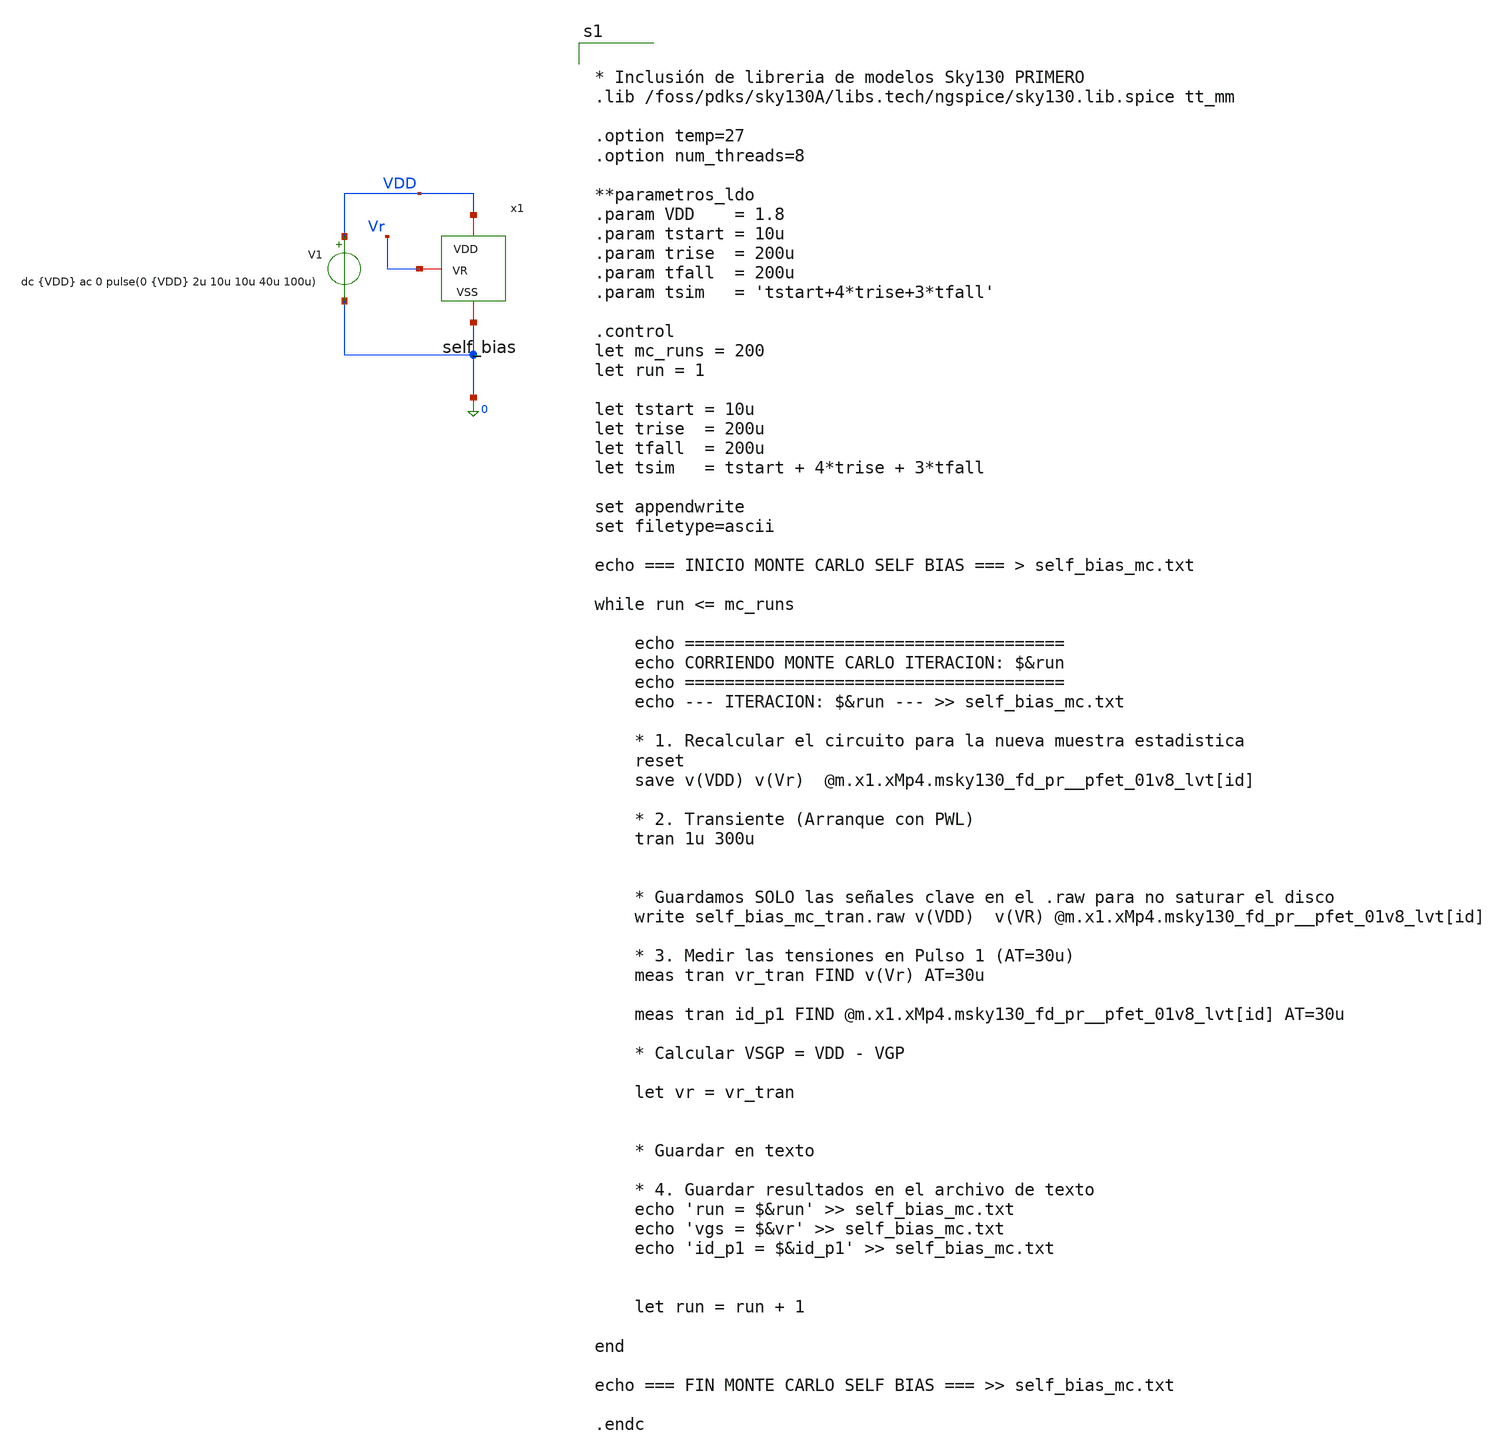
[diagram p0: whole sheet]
** sch_path: xschem/Iref/self_bias_tb_mc.sch
**.subckt self_bias_tb_mc
V1 VDD 0 dc {VDD} ac 0 pulse(0 {VDD} 2u 10u 10u 40u 100u)
x1 VDD Vr 0 self_bias
**** begin user architecture code


* Inclusión de libreria de modelos Sky130 PRIMERO
.lib /foss/pdks/sky130A/libs.tech/ngspice/sky130.lib.spice tt_mm

.option temp=27
.option num_threads=8

**parametros_ldo
.param VDD    = 1.8
.param tstart = 10u
.param trise  = 200u
.param tfall  = 200u
.param tsim   = 'tstart+4*trise+3*tfall'

.control
let mc_runs = 200
let run = 1

let tstart = 10u
let trise  = 200u
let tfall  = 200u
let tsim   = tstart + 4*trise + 3*tfall

set appendwrite
set filetype=ascii

echo === INICIO MONTE CARLO SELF BIAS === > self_bias_mc.txt

while run <= mc_runs

    echo ======================================
    echo CORRIENDO MONTE CARLO ITERACION: $&run
    echo ======================================
    echo --- ITERACION: $&run --- >> self_bias_mc.txt

    * 1. Recalcular el circuito para la nueva muestra estadistica
    reset
    save v(VDD) v(Vr)  @m.x1.xMp4.msky130_fd_pr__pfet_01v8_lvt[id]

    * 2. Transiente (Arranque con PWL)
    tran 1u 300u


    * Guardamos SOLO las señales clave en el .raw para no saturar el disco
    write self_bias_mc_tran.raw v(VDD)  v(VR) @m.x1.xMp4.msky130_fd_pr__pfet_01v8_lvt[id]

    * 3. Medir las tensiones en Pulso 1 (AT=30u)
    meas tran vr_tran FIND v(Vr) AT=30u

    meas tran id_p1 FIND @m.x1.xMp4.msky130_fd_pr__pfet_01v8_lvt[id] AT=30u

    * Calcular VSGP = VDD - VGP

    let vr = vr_tran


    * Guardar en texto

    * 4. Guardar resultados en el archivo de texto
    echo 'run = $&run' >> self_bias_mc.txt
    echo 'vgs = $&vr' >> self_bias_mc.txt
    echo 'id_p1 = $&id_p1' >> self_bias_mc.txt


    let run = run + 1

end

echo === FIN MONTE CARLO SELF BIAS === >> self_bias_mc.txt

.endc


**** end user architecture code
**.ends

* expanding   symbol:  self_bias.sym # of pins=3
** sym_path: xschem/Iref/self_bias.sym
** sch_path: xschem/Iref/self_bias.sch
.subckt self_bias VDD VR VSS
*.iopin VR
*.iopin VDD
*.iopin VSS
XMp4 Vgp Vgp VDD VDD sky130_fd_pr__pfet_01v8_lvt L=1 W=30 nf=1 ad='int((1 + 1)/2) * 30 / 1 * 0.29' as='int((1 + 2)/2) * 30 / 1 * 0.29'
+ pd='2*int((1 + 1)/2) * (30 / 1 + 0.29)' ps='2*int((1 + 2)/2) * (30 / 1 + 0.29)' nrd='0.29 / 30 ' nrs='0.29 / 30 '
+ sa=0 sb=0 sd=0 mult=1 m=1
XMp3 VDI Vgp VDD VDD sky130_fd_pr__pfet_01v8_lvt L=1 W=30 nf=1 ad='int((1 + 1)/2) * 30 / 1 * 0.29' as='int((1 + 2)/2) * 30 / 1 * 0.29'
+ pd='2*int((1 + 1)/2) * (30 / 1 + 0.29)' ps='2*int((1 + 2)/2) * (30 / 1 + 0.29)' nrd='0.29 / 30 ' nrs='0.29 / 30 '
+ sa=0 sb=0 sd=0 mult=1 m=1
XMs2 VDinv VR VDD VDD sky130_fd_pr__pfet_01v8_lvt L=25 W=0.5 nf=1 ad='int((1 + 1)/2) * 0.5 / 1 * 0.29'
+ as='int((1 + 2)/2) * 0.5 / 1 * 0.29' pd='2*int((1 + 1)/2) * (0.5 / 1 + 0.29)' ps='2*int((1 + 2)/2) * (0.5 / 1 + 0.29)'
+ nrd='0.29 / 0.5 ' nrs='0.29 / 0.5 ' sa=0 sb=0 sd=0 mult=1 m=1
XR4 VSS VR VSS sky130_fd_pr__res_iso_pw W=0.7 L=11 m=1
XMn2 Vgp VDI VR VSS sky130_fd_pr__nfet_01v8 L=1 W=20 nf=1 ad='int((1 + 1)/2) * 20 / 1 * 0.29' as='int((1 + 2)/2) * 20 / 1 * 0.29'
+ pd='2*int((1 + 1)/2) * (20 / 1 + 0.29)' ps='2*int((1 + 2)/2) * (20 / 1 + 0.29)' nrd='0.29 / 20 ' nrs='0.29 / 20 '
+ sa=0 sb=0 sd=0 mult=1 m=1
XMn1 VDI VR VSS VSS sky130_fd_pr__nfet_01v8 L=1 W=5 nf=1 ad='int((1 + 1)/2) * 5 / 1 * 0.29' as='int((1 + 2)/2) * 5 / 1 * 0.29'
+ pd='2*int((1 + 1)/2) * (5 / 1 + 0.29)' ps='2*int((1 + 2)/2) * (5 / 1 + 0.29)' nrd='0.29 / 5 ' nrs='0.29 / 5 '
+ sa=0 sb=0 sd=0 mult=1 m=1
XMs3 VDinv VR VSS VSS sky130_fd_pr__nfet_01v8 L=1 W=20 nf=1 ad='int((1 + 1)/2) * 20 / 1 * 0.29' as='int((1 + 2)/2) * 20 / 1 * 0.29'
+ pd='2*int((1 + 1)/2) * (20 / 1 + 0.29)' ps='2*int((1 + 2)/2) * (20 / 1 + 0.29)' nrd='0.29 / 20 ' nrs='0.29 / 20 '
+ sa=0 sb=0 sd=0 mult=1 m=1
XMs1 Vgp VDinv VSS VSS sky130_fd_pr__nfet_01v8 L=1 W=2 nf=1 ad='int((1 + 1)/2) * 2 / 1 * 0.29' as='int((1 + 2)/2) * 2 / 1 * 0.29'
+ pd='2*int((1 + 1)/2) * (2 / 1 + 0.29)' ps='2*int((1 + 2)/2) * (2 / 1 + 0.29)' nrd='0.29 / 2 ' nrs='0.29 / 2 '
+ sa=0 sb=0 sd=0 mult=1 m=1
.ends

.end
